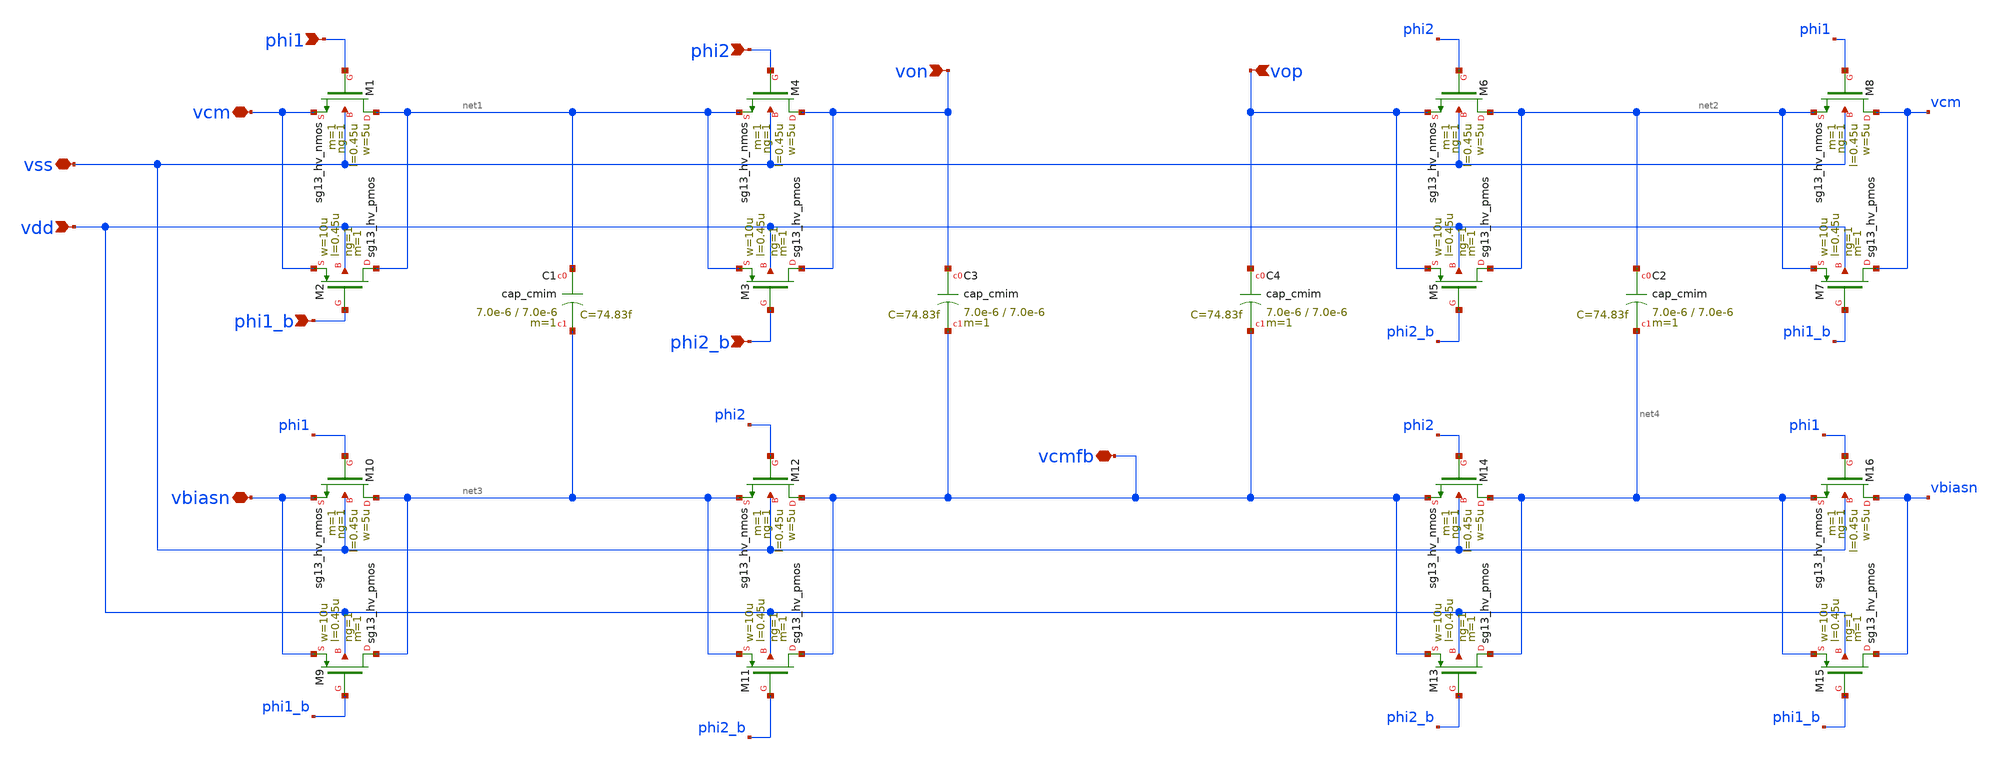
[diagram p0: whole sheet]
** sch_path: 3_real_circuits/sc_cmfb_cmos.sch
**.subckt sc_cmfb_cmos von vop phi2_b phi2 phi1_b phi1 vdd vss vbiasn vcm vcmfb
*.ipin von
*.ipin vop
*.ipin phi2_b
*.ipin phi2
*.ipin phi1_b
*.ipin phi1
*.ipin vdd
*.iopin vss
*.iopin vbiasn
*.iopin vcm
*.iopin vcmfb
XC1 net1 net3 cap_cmim w=7.0e-6 l=7.0e-6 m=1 mm_ok=1
XC3 von vcmfb cap_cmim w=7.0e-6 l=7.0e-6 m=1 mm_ok=1
XC4 vop vcmfb cap_cmim w=7.0e-6 l=7.0e-6 m=1 mm_ok=1
XC2 net2 net4 cap_cmim w=7.0e-6 l=7.0e-6 m=1 mm_ok=1
XM2 net1 phi1_b vcm vdd sg13_hv_pmos w=10u l=0.45u ng=1 m=1 mm_ok=1
XM1 net1 phi1 vcm vss sg13_hv_nmos w=5u l=0.45u ng=1 m=1 mm_ok=1
XM3 von phi2_b net1 vdd sg13_hv_pmos w=10u l=0.45u ng=1 m=1 mm_ok=1
XM4 von phi2 net1 vss sg13_hv_nmos w=5u l=0.45u ng=1 m=1 mm_ok=1
XM5 net2 phi2_b vop vdd sg13_hv_pmos w=10u l=0.45u ng=1 m=1 mm_ok=1
XM6 net2 phi2 vop vss sg13_hv_nmos w=5u l=0.45u ng=1 m=1 mm_ok=1
XM7 vcm phi1_b net2 vdd sg13_hv_pmos w=10u l=0.45u ng=1 m=1 mm_ok=1
XM8 vcm phi1 net2 vss sg13_hv_nmos w=5u l=0.45u ng=1 m=1 mm_ok=1
XM9 net3 phi1_b vbiasn vdd sg13_hv_pmos w=10u l=0.45u ng=1 m=1 mm_ok=1
XM10 net3 phi1 vbiasn vss sg13_hv_nmos w=5u l=0.45u ng=1 m=1 mm_ok=1
XM11 vcmfb phi2_b net3 vdd sg13_hv_pmos w=10u l=0.45u ng=1 m=1 mm_ok=1
XM12 vcmfb phi2 net3 vss sg13_hv_nmos w=5u l=0.45u ng=1 m=1 mm_ok=1
XM13 net4 phi2_b vcmfb vdd sg13_hv_pmos w=10u l=0.45u ng=1 m=1 mm_ok=1
XM14 net4 phi2 vcmfb vss sg13_hv_nmos w=5u l=0.45u ng=1 m=1 mm_ok=1
XM15 vbiasn phi1_b net4 vdd sg13_hv_pmos w=10u l=0.45u ng=1 m=1 mm_ok=1
XM16 vbiasn phi1 net4 vss sg13_hv_nmos w=5u l=0.45u ng=1 m=1 mm_ok=1
**.ends
.end
